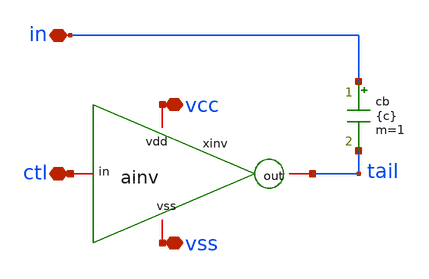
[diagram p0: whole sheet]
** sch_path: samples/digital_cosimulation/ccap/symbol/ccap.sch
**.subckt ccap ctl in vcc vss
*.iopin ctl
*.iopin in
*.iopin vcc
*.iopin vss
xinv ctl tail vcc vss ainv
cb in tail {c} m=1
**.ends

* expanding   symbol:  symbol/ainv.sym # of pins=4
** sym_path: samples/digital_cosimulation/ainv/symbol/ainv.sym
** sch_path: samples/digital_cosimulation/ainv/symbol/ainv.sch
.subckt ainv in out vdd vss
*.iopin vdd
*.iopin out
*.iopin vss
*.iopin in
**** begin user architecture code


.model p1 pmos   level=2 vto=-0.5 kp=8.5e-6 gamma=0.4 phi=0.65 lambda=0.05 xj=0.5e-6
.model n1 nmos   level=2 vto=0.5 kp=24e-6 gamma=0.15 phi=0.65 lambda=0.015 xj=0.5e-6


**** end user architecture code
mn out in vss vss n1 w=5u l=0.18u m=1
mp out in vdd vdd p1 w=5u l=0.18u m=1
.ends

.end
